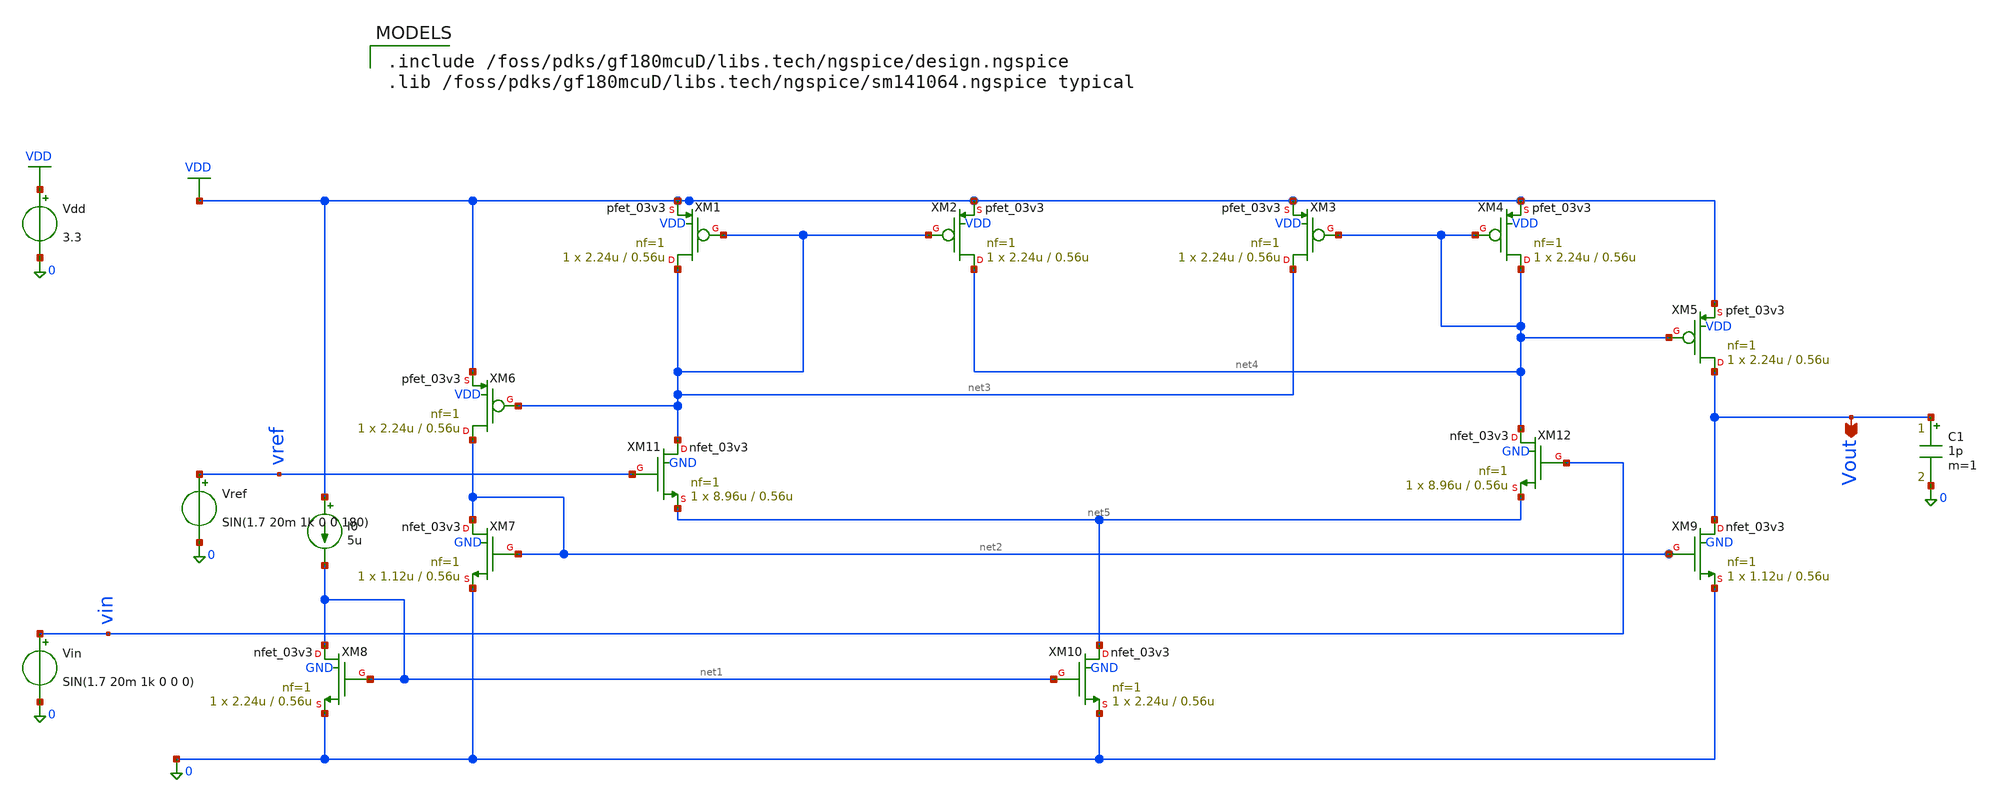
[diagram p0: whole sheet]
** sch_path: comparator/schematic-design/comparator_2_ac.sch
**.subckt comparator_2_ac Vout
*.opin Vout
XM1 net3 net3 VDD VDD pfet_03v3 L=0.56u W=2.24u nf=1 ad='int((nf+1)/2) * W/nf * 0.18u' as='int((nf+2)/2) * W/nf * 0.18u'
+ pd='2*int((nf+1)/2) * (W/nf + 0.18u)' ps='2*int((nf+2)/2) * (W/nf + 0.18u)' nrd='0.18u / W' nrs='0.18u / W'
+ sa=0 sb=0 sd=0 m=1 par=1
XM2 net4 net3 VDD VDD pfet_03v3 L=0.56u W=2.24u nf=1 ad='int((nf+1)/2) * W/nf * 0.18u' as='int((nf+2)/2) * W/nf * 0.18u'
+ pd='2*int((nf+1)/2) * (W/nf + 0.18u)' ps='2*int((nf+2)/2) * (W/nf + 0.18u)' nrd='0.18u / W' nrs='0.18u / W'
+ sa=0 sb=0 sd=0 m=1 par=1
XM3 net3 net4 VDD VDD pfet_03v3 L=0.56u W=2.24u nf=1 ad='int((nf+1)/2) * W/nf * 0.18u' as='int((nf+2)/2) * W/nf * 0.18u'
+ pd='2*int((nf+1)/2) * (W/nf + 0.18u)' ps='2*int((nf+2)/2) * (W/nf + 0.18u)' nrd='0.18u / W' nrs='0.18u / W'
+ sa=0 sb=0 sd=0 m=1 par=1
XM4 net4 net4 VDD VDD pfet_03v3 L=0.56u W=2.24u nf=1 ad='int((nf+1)/2) * W/nf * 0.18u' as='int((nf+2)/2) * W/nf * 0.18u'
+ pd='2*int((nf+1)/2) * (W/nf + 0.18u)' ps='2*int((nf+2)/2) * (W/nf + 0.18u)' nrd='0.18u / W' nrs='0.18u / W'
+ sa=0 sb=0 sd=0 m=1 par=1
XM5 Vout net4 VDD VDD pfet_03v3 L=0.56u W=2.24u nf=1 ad='int((nf+1)/2) * W/nf * 0.18u' as='int((nf+2)/2) * W/nf * 0.18u'
+ pd='2*int((nf+1)/2) * (W/nf + 0.18u)' ps='2*int((nf+2)/2) * (W/nf + 0.18u)' nrd='0.18u / W' nrs='0.18u / W'
+ sa=0 sb=0 sd=0 m=1 par=1
XM6 net2 net3 VDD VDD pfet_03v3 L=0.56u W=2.24u nf=1 ad='int((nf+1)/2) * W/nf * 0.18u' as='int((nf+2)/2) * W/nf * 0.18u'
+ pd='2*int((nf+1)/2) * (W/nf + 0.18u)' ps='2*int((nf+2)/2) * (W/nf + 0.18u)' nrd='0.18u / W' nrs='0.18u / W'
+ sa=0 sb=0 sd=0 m=1 par=1
XM7 net2 net2 0 GND nfet_03v3 L=0.56u W=1.12u nf=1 ad='int((nf+1)/2) * W/nf * 0.18u' as='int((nf+2)/2) * W/nf * 0.18u'
+ pd='2*int((nf+1)/2) * (W/nf + 0.18u)' ps='2*int((nf+2)/2) * (W/nf + 0.18u)' nrd='0.18u / W' nrs='0.18u / W'
+ sa=0 sb=0 sd=0 m=1 par=1
XM8 net1 net1 0 GND nfet_03v3 L=0.56u W=2.24u nf=1 ad='int((nf+1)/2) * W/nf * 0.18u' as='int((nf+2)/2) * W/nf * 0.18u'
+ pd='2*int((nf+1)/2) * (W/nf + 0.18u)' ps='2*int((nf+2)/2) * (W/nf + 0.18u)' nrd='0.18u / W' nrs='0.18u / W'
+ sa=0 sb=0 sd=0 m=1 par=1
XM9 Vout net2 0 GND nfet_03v3 L=0.56u W=1.12u nf=1 ad='int((nf+1)/2) * W/nf * 0.18u' as='int((nf+2)/2) * W/nf * 0.18u'
+ pd='2*int((nf+1)/2) * (W/nf + 0.18u)' ps='2*int((nf+2)/2) * (W/nf + 0.18u)' nrd='0.18u / W' nrs='0.18u / W'
+ sa=0 sb=0 sd=0 m=1 par=1
XM10 net5 net1 0 GND nfet_03v3 L=0.56u W=2.24u nf=1 ad='int((nf+1)/2) * W/nf * 0.18u' as='int((nf+2)/2) * W/nf * 0.18u'
+ pd='2*int((nf+1)/2) * (W/nf + 0.18u)' ps='2*int((nf+2)/2) * (W/nf + 0.18u)' nrd='0.18u / W' nrs='0.18u / W'
+ sa=0 sb=0 sd=0 m=1 par=1
XM11 net3 vref net5 GND nfet_03v3 L=0.56u W=8.96u nf=1 ad='int((nf+1)/2) * W/nf * 0.18u' as='int((nf+2)/2) * W/nf * 0.18u'
+ pd='2*int((nf+1)/2) * (W/nf + 0.18u)' ps='2*int((nf+2)/2) * (W/nf + 0.18u)' nrd='0.18u / W' nrs='0.18u / W'
+ sa=0 sb=0 sd=0 m=1 par=1
XM12 net4 vin net5 GND nfet_03v3 L=0.56u W=8.96u nf=1 ad='int((nf+1)/2) * W/nf * 0.18u' as='int((nf+2)/2) * W/nf * 0.18u'
+ pd='2*int((nf+1)/2) * (W/nf + 0.18u)' ps='2*int((nf+2)/2) * (W/nf + 0.18u)' nrd='0.18u / W' nrs='0.18u / W'
+ sa=0 sb=0 sd=0 m=1 par=1
I0 VDD net1 5u
Vref vref 0 SIN(1.7 20m 1k 0 0 180)
Vin vin 0 SIN(1.7 20m 1k 0 0 0)

Vdd VDD 0 3.3
C1 Vout 0 1p m=1
**** begin user architecture code

.include /foss/pdks/gf180mcuD/libs.tech/ngspice/design.ngspice
.lib /foss/pdks/gf180mcuD/libs.tech/ngspice/sm141064.ngspice typical


.control

set noaskquit
save all

tran 1u 4m

let vdiff = v(vin)-v(vref)

write comparator_two_sine.raw all

* Plot 1: two opposite-phase comparator inputs
plot v(vin) v(vref) title 'Comparator Differential Inputs'

* Plot 2: differential input voltage
plot vdiff title 'Differential Input: Vin - Vref'

* Plot 3: comparator output
plot v(vout) title 'Comparator Output'

* Plot 4: inputs and output together
plot v(vin) v(vref) v(vout) title 'Comparator Transient Response'

* Plot 5: output versus differential input
plot v(vout) vs vdiff title 'Comparator Transfer Characteristic'

.endc

**** end user architecture code
**.ends
.GLOBAL VDD
.end
